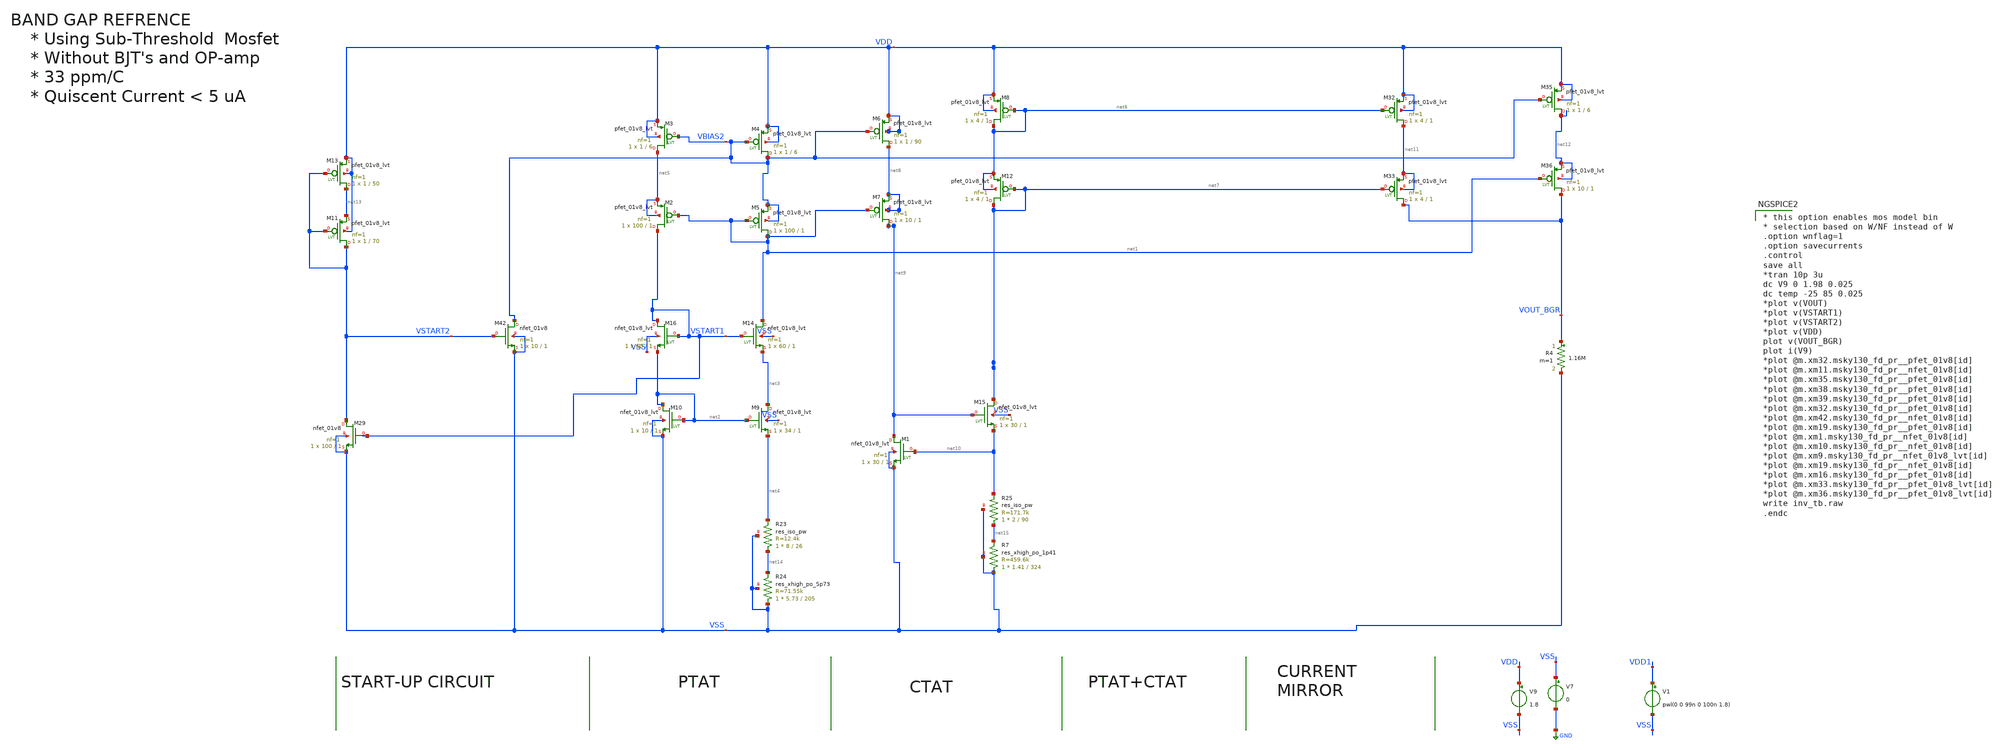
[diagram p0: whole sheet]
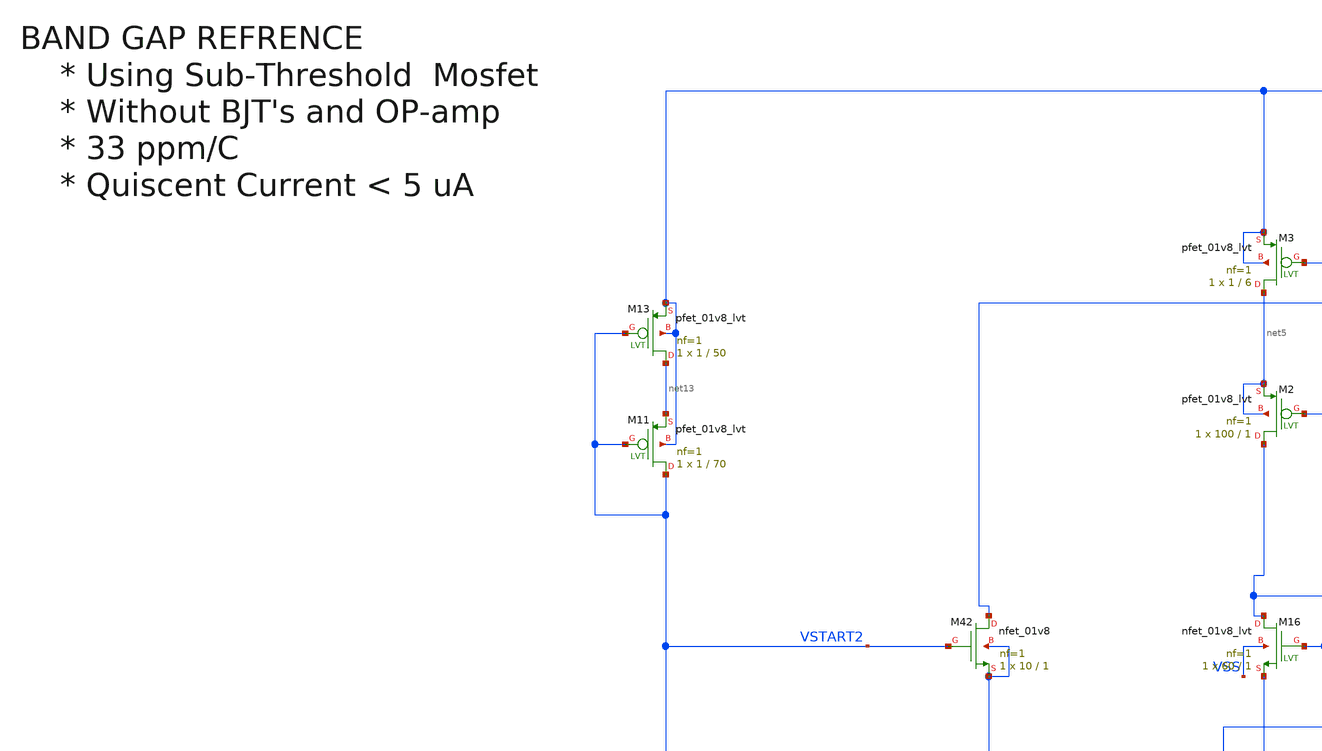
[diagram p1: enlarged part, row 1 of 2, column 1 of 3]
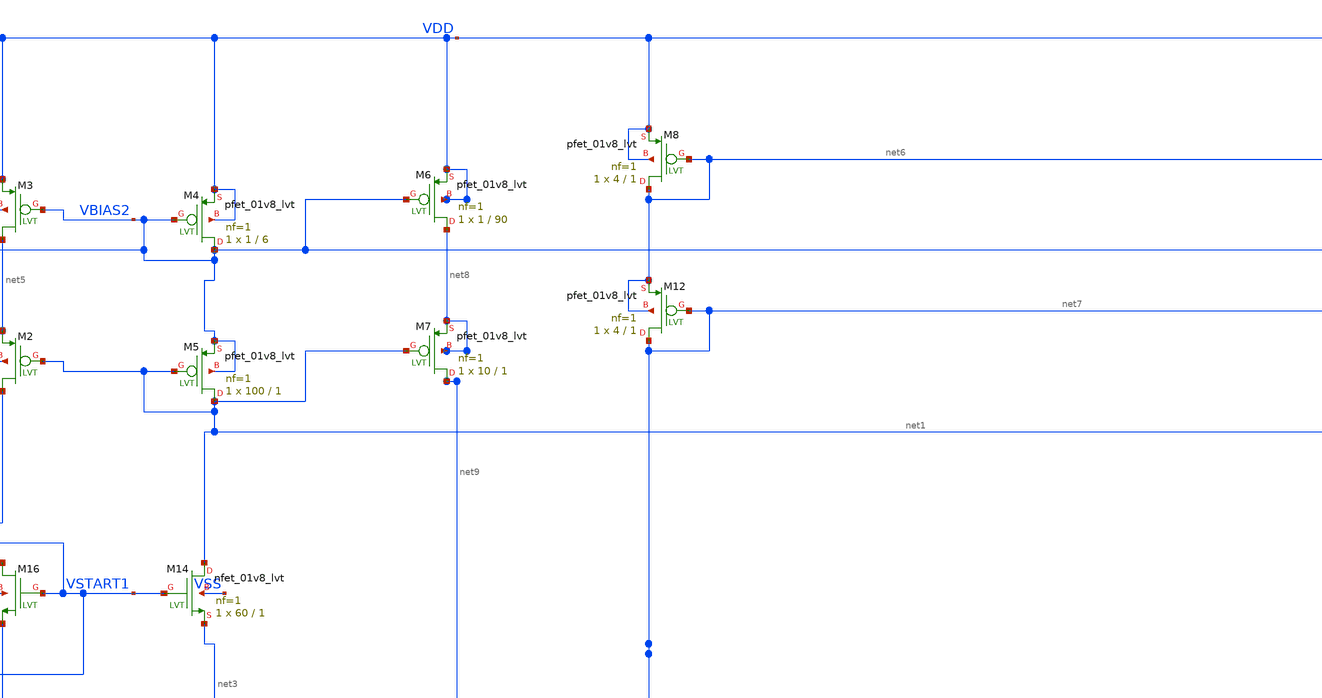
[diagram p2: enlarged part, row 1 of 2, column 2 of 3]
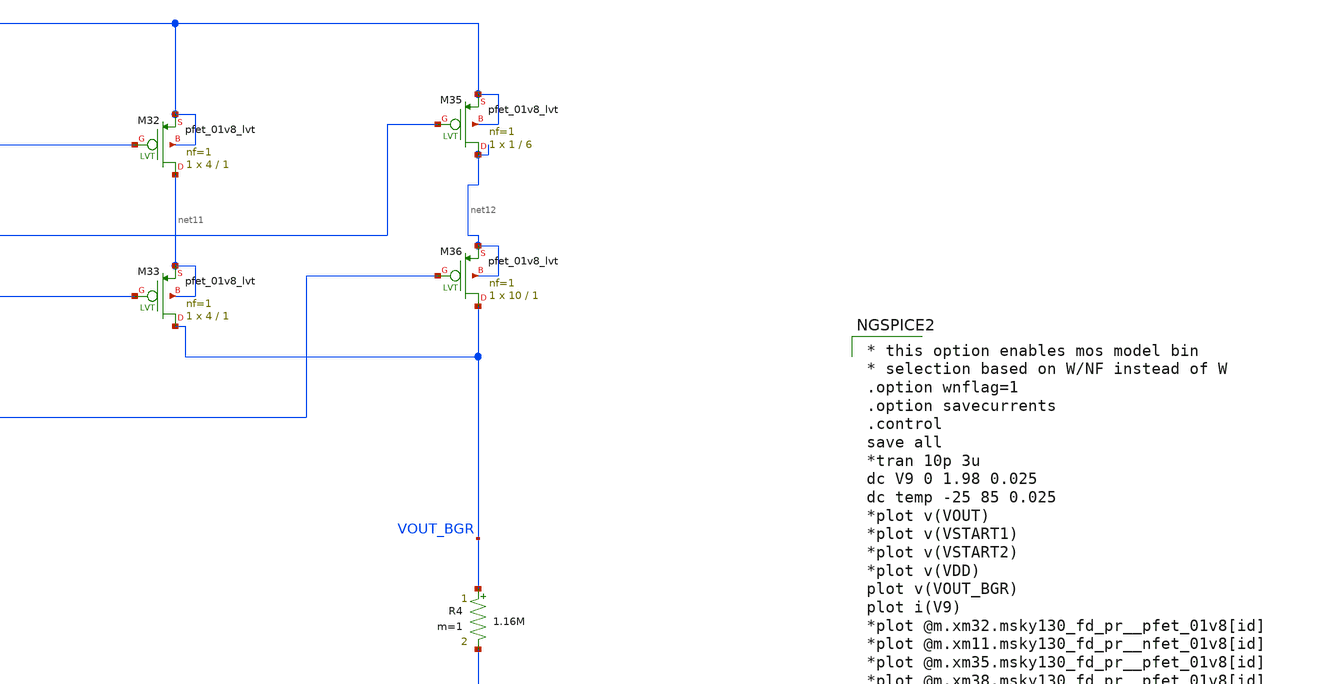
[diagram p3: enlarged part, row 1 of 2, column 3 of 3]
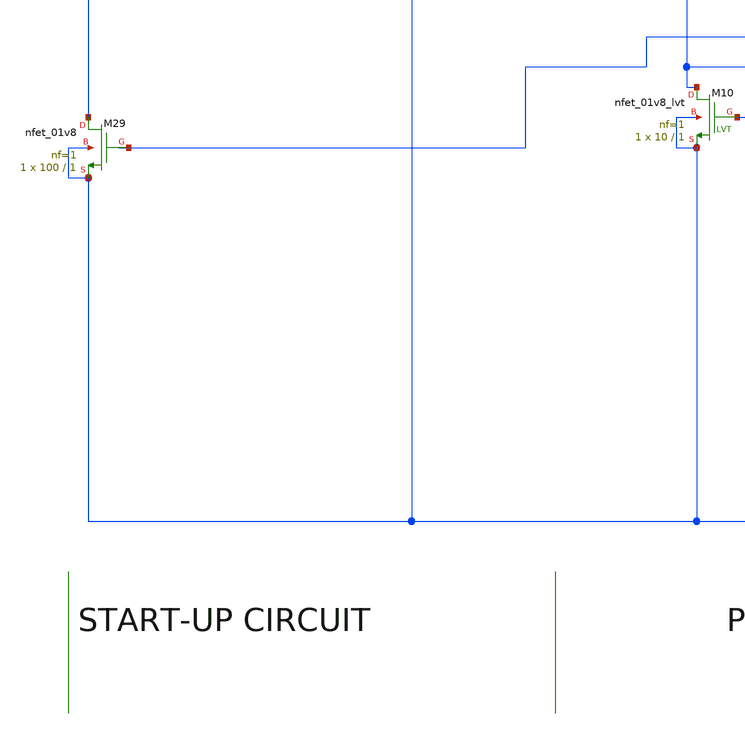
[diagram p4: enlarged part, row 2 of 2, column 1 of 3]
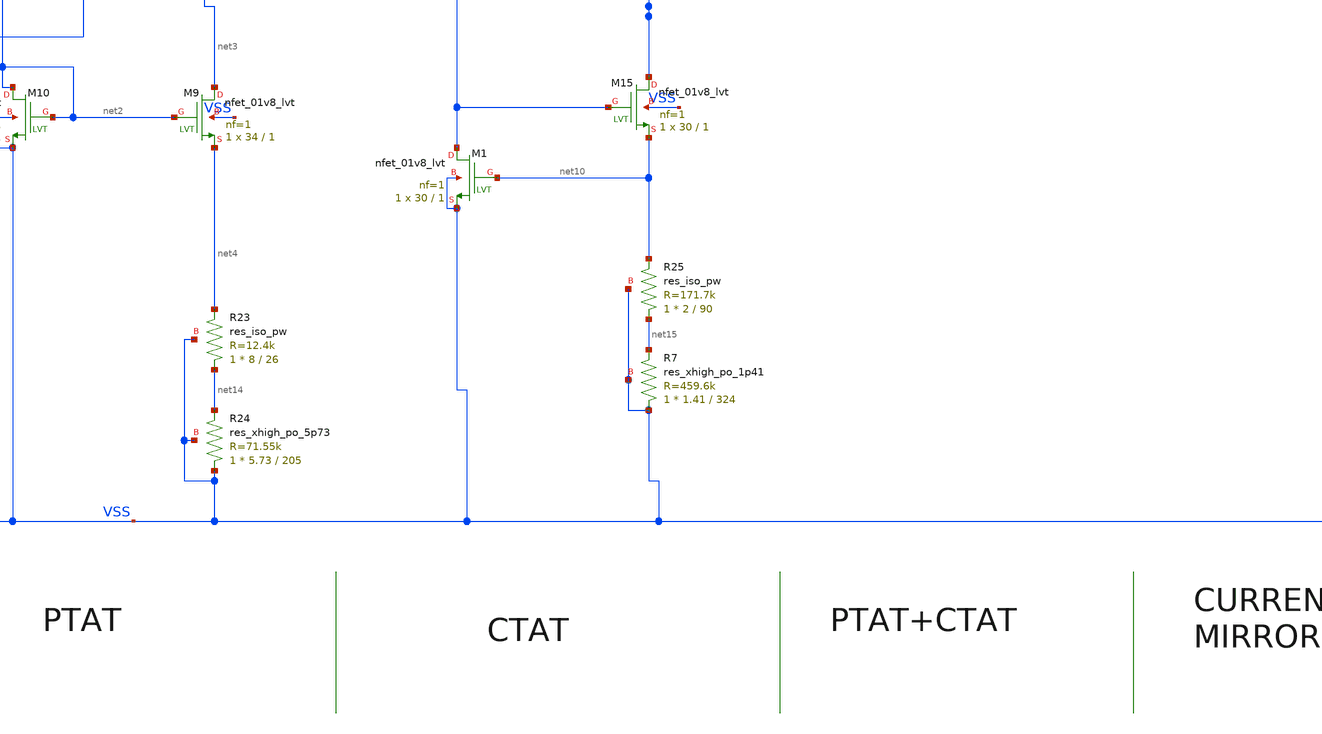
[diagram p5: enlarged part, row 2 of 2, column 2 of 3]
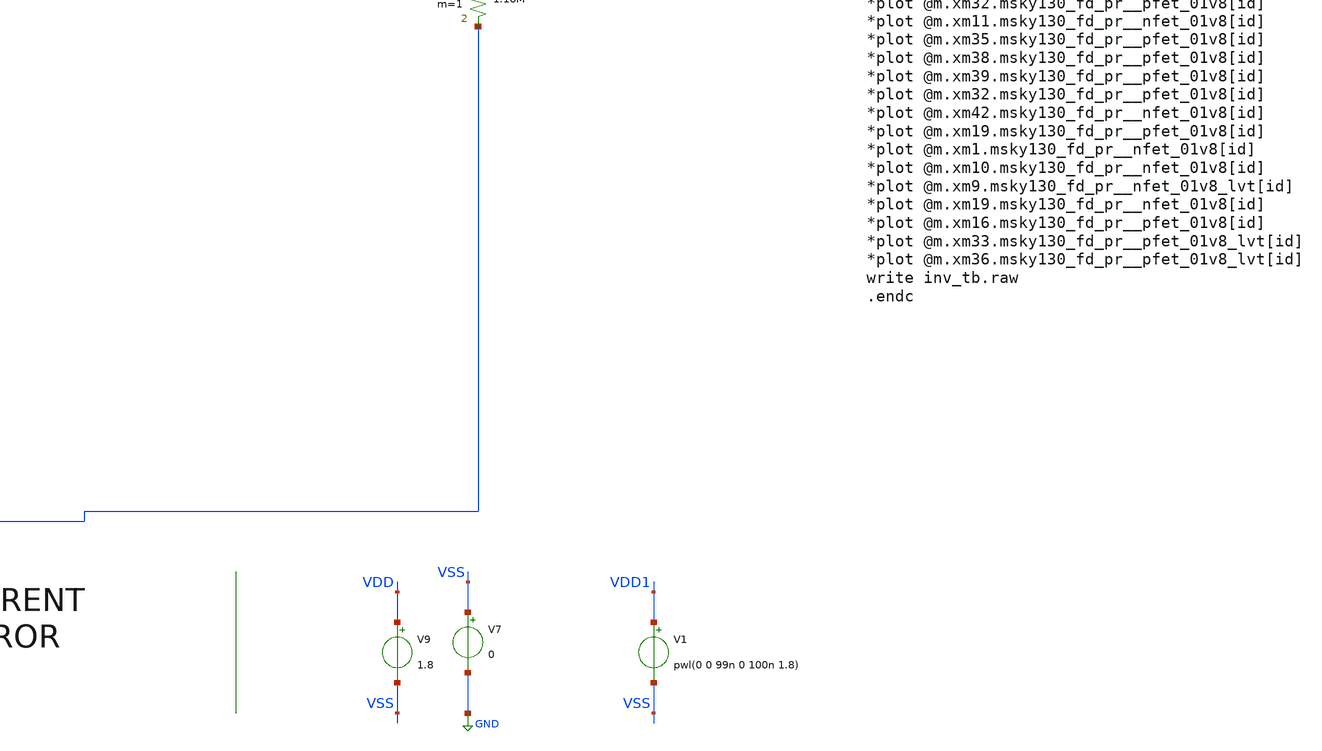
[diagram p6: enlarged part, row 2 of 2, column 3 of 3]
** sch_path: bgr_quiscent_current.sch
**.subckt bgr_quiscent_current
V7 VSS GND 0
V9 VDD VSS 1.8
XM29 VSTART2 VSTART1 VSS VSS sky130_fd_pr__nfet_01v8 L=1 W=100 nf=1 ad='int((nf+1)/2) * W/nf * 0.29'
+ as='int((nf+2)/2) * W/nf * 0.29' pd='2*int((nf+1)/2) * (W/nf + 0.29)' ps='2*int((nf+2)/2) * (W/nf + 0.29)'
+ nrd='0.29 / W' nrs='0.29 / W' sa=0 sb=0 sd=0 mult=1 m=1
XM42 VBIAS2 VSTART2 VSS VSS sky130_fd_pr__nfet_01v8 L=1 W=10 nf=1 ad='int((nf+1)/2) * W/nf * 0.29' as='int((nf+2)/2) * W/nf * 0.29'
+ pd='2*int((nf+1)/2) * (W/nf + 0.29)' ps='2*int((nf+2)/2) * (W/nf + 0.29)' nrd='0.29 / W' nrs='0.29 / W'
+ sa=0 sb=0 sd=0 mult=1 m=1
XM3 net5 VBIAS2 VDD VDD sky130_fd_pr__pfet_01v8_lvt L=6 W=1 nf=1 ad='int((nf+1)/2) * W/nf * 0.29' as='int((nf+2)/2) * W/nf * 0.29'
+ pd='2*int((nf+1)/2) * (W/nf + 0.29)' ps='2*int((nf+2)/2) * (W/nf + 0.29)' nrd='0.29 / W' nrs='0.29 / W'
+ sa=0 sb=0 sd=0 mult=1 m=1
XM2 VSTART1 net1 net5 net5 sky130_fd_pr__pfet_01v8_lvt L=1 W=100 nf=1 ad='int((nf+1)/2) * W/nf * 0.29'
+ as='int((nf+2)/2) * W/nf * 0.29' pd='2*int((nf+1)/2) * (W/nf + 0.29)' ps='2*int((nf+2)/2) * (W/nf + 0.29)'
+ nrd='0.29 / W' nrs='0.29 / W' sa=0 sb=0 sd=0 mult=1 m=1
XM4 VBIAS2 VBIAS2 VDD VDD sky130_fd_pr__pfet_01v8_lvt L=6 W=1 nf=1 ad='int((nf+1)/2) * W/nf * 0.29' as='int((nf+2)/2) * W/nf * 0.29'
+ pd='2*int((nf+1)/2) * (W/nf + 0.29)' ps='2*int((nf+2)/2) * (W/nf + 0.29)' nrd='0.29 / W' nrs='0.29 / W'
+ sa=0 sb=0 sd=0 mult=1 m=1
XM5 net1 net1 VBIAS2 VBIAS2 sky130_fd_pr__pfet_01v8_lvt L=1 W=100 nf=1 ad='int((nf+1)/2) * W/nf * 0.29'
+ as='int((nf+2)/2) * W/nf * 0.29' pd='2*int((nf+1)/2) * (W/nf + 0.29)' ps='2*int((nf+2)/2) * (W/nf + 0.29)'
+ nrd='0.29 / W' nrs='0.29 / W' sa=0 sb=0 sd=0 mult=1 m=1
XM6 net8 VBIAS2 VDD VDD sky130_fd_pr__pfet_01v8_lvt L=90 W=1 nf=1 ad='int((nf+1)/2) * W/nf * 0.29' as='int((nf+2)/2) * W/nf * 0.29'
+ pd='2*int((nf+1)/2) * (W/nf + 0.29)' ps='2*int((nf+2)/2) * (W/nf + 0.29)' nrd='0.29 / W' nrs='0.29 / W'
+ sa=0 sb=0 sd=0 mult=1 m=1
XM7 net9 net1 net8 net8 sky130_fd_pr__pfet_01v8_lvt L=1 W=10 nf=1 ad='int((nf+1)/2) * W/nf * 0.29' as='int((nf+2)/2) * W/nf * 0.29'
+ pd='2*int((nf+1)/2) * (W/nf + 0.29)' ps='2*int((nf+2)/2) * (W/nf + 0.29)' nrd='0.29 / W' nrs='0.29 / W'
+ sa=0 sb=0 sd=0 mult=1 m=1
XM8 net6 net6 VDD VDD sky130_fd_pr__pfet_01v8_lvt L=1 W=4 nf=1 ad='int((nf+1)/2) * W/nf * 0.29' as='int((nf+2)/2) * W/nf * 0.29'
+ pd='2*int((nf+1)/2) * (W/nf + 0.29)' ps='2*int((nf+2)/2) * (W/nf + 0.29)' nrd='0.29 / W' nrs='0.29 / W'
+ sa=0 sb=0 sd=0 mult=1 m=1
XM12 net7 net7 net6 net6 sky130_fd_pr__pfet_01v8_lvt L=1 W=4 nf=1 ad='int((nf+1)/2) * W/nf * 0.29' as='int((nf+2)/2) * W/nf * 0.29'
+ pd='2*int((nf+1)/2) * (W/nf + 0.29)' ps='2*int((nf+2)/2) * (W/nf + 0.29)' nrd='0.29 / W' nrs='0.29 / W'
+ sa=0 sb=0 sd=0 mult=1 m=1
XM32 net11 net6 VDD VDD sky130_fd_pr__pfet_01v8_lvt L=1 W=4 nf=1 ad='int((nf+1)/2) * W/nf * 0.29' as='int((nf+2)/2) * W/nf * 0.29'
+ pd='2*int((nf+1)/2) * (W/nf + 0.29)' ps='2*int((nf+2)/2) * (W/nf + 0.29)' nrd='0.29 / W' nrs='0.29 / W'
+ sa=0 sb=0 sd=0 mult=1 m=1
XM33 VOUT_BGR net7 net11 net11 sky130_fd_pr__pfet_01v8_lvt L=1 W=4 nf=1 ad='int((nf+1)/2) * W/nf * 0.29'
+ as='int((nf+2)/2) * W/nf * 0.29' pd='2*int((nf+1)/2) * (W/nf + 0.29)' ps='2*int((nf+2)/2) * (W/nf + 0.29)'
+ nrd='0.29 / W' nrs='0.29 / W' sa=0 sb=0 sd=0 mult=1 m=1
XM35 net12 VBIAS2 VDD VDD sky130_fd_pr__pfet_01v8_lvt L=6 W=1 nf=1 ad='int((nf+1)/2) * W/nf * 0.29' as='int((nf+2)/2) * W/nf * 0.29'
+ pd='2*int((nf+1)/2) * (W/nf + 0.29)' ps='2*int((nf+2)/2) * (W/nf + 0.29)' nrd='0.29 / W' nrs='0.29 / W'
+ sa=0 sb=0 sd=0 mult=1 m=1
XM36 VOUT_BGR net1 net12 net12 sky130_fd_pr__pfet_01v8_lvt L=1 W=10 nf=1 ad='int((nf+1)/2) * W/nf * 0.29'
+ as='int((nf+2)/2) * W/nf * 0.29' pd='2*int((nf+1)/2) * (W/nf + 0.29)' ps='2*int((nf+2)/2) * (W/nf + 0.29)'
+ nrd='0.29 / W' nrs='0.29 / W' sa=0 sb=0 sd=0 mult=1 m=1
R4 VOUT_BGR VSS 1.16M m=1
XM11 VSTART2 VSTART2 net13 VDD sky130_fd_pr__pfet_01v8_lvt L=70 W=1 nf=1 ad='int((nf+1)/2) * W/nf * 0.29'
+ as='int((nf+2)/2) * W/nf * 0.29' pd='2*int((nf+1)/2) * (W/nf + 0.29)' ps='2*int((nf+2)/2) * (W/nf + 0.29)'
+ nrd='0.29 / W' nrs='0.29 / W' sa=0 sb=0 sd=0 mult=1 m=1
XM13 net13 VSTART2 VDD VDD sky130_fd_pr__pfet_01v8_lvt L=50 W=1 nf=1 ad='int((nf+1)/2) * W/nf * 0.29'
+ as='int((nf+2)/2) * W/nf * 0.29' pd='2*int((nf+1)/2) * (W/nf + 0.29)' ps='2*int((nf+2)/2) * (W/nf + 0.29)'
+ nrd='0.29 / W' nrs='0.29 / W' sa=0 sb=0 sd=0 mult=1 m=1
V1 VDD1 VSS pwl(0 0 99n 0 100n 1.8)
XR23 net14 net4 VSS sky130_fd_pr__res_iso_pw W=8 L=26 m=1
XR24 VSS net14 VSS sky130_fd_pr__res_xhigh_po_5p73 L=205 mult=1 m=1
XR25 net15 net10 VSS sky130_fd_pr__res_iso_pw W=2 L=90 m=1
XM14 net1 VSTART1 net3 VSS sky130_fd_pr__nfet_01v8_lvt L=1 W=60 nf=1 ad='int((nf+1)/2) * W/nf * 0.29'
+ as='int((nf+2)/2) * W/nf * 0.29' pd='2*int((nf+1)/2) * (W/nf + 0.29)' ps='2*int((nf+2)/2) * (W/nf + 0.29)'
+ nrd='0.29 / W' nrs='0.29 / W' sa=0 sb=0 sd=0 mult=1 m=1
XM16 VSTART1 VSTART1 net2 VSS sky130_fd_pr__nfet_01v8_lvt L=1 W=60 nf=1 ad='int((nf+1)/2) * W/nf * 0.29'
+ as='int((nf+2)/2) * W/nf * 0.29' pd='2*int((nf+1)/2) * (W/nf + 0.29)' ps='2*int((nf+2)/2) * (W/nf + 0.29)'
+ nrd='0.29 / W' nrs='0.29 / W' sa=0 sb=0 sd=0 mult=1 m=1
XM9 net3 net2 net4 VSS sky130_fd_pr__nfet_01v8_lvt L=1 W=34 nf=1 ad='int((nf+1)/2) * W/nf * 0.29' as='int((nf+2)/2) * W/nf * 0.29'
+ pd='2*int((nf+1)/2) * (W/nf + 0.29)' ps='2*int((nf+2)/2) * (W/nf + 0.29)' nrd='0.29 / W' nrs='0.29 / W'
+ sa=0 sb=0 sd=0 mult=1 m=1
XM10 net2 net2 VSS VSS sky130_fd_pr__nfet_01v8_lvt L=1 W=10 nf=1 ad='int((nf+1)/2) * W/nf * 0.29' as='int((nf+2)/2) * W/nf * 0.29'
+ pd='2*int((nf+1)/2) * (W/nf + 0.29)' ps='2*int((nf+2)/2) * (W/nf + 0.29)' nrd='0.29 / W' nrs='0.29 / W'
+ sa=0 sb=0 sd=0 mult=1 m=1
XM1 net9 net10 VSS VSS sky130_fd_pr__nfet_01v8_lvt L=1 W=30 nf=1 ad='int((nf+1)/2) * W/nf * 0.29' as='int((nf+2)/2) * W/nf * 0.29'
+ pd='2*int((nf+1)/2) * (W/nf + 0.29)' ps='2*int((nf+2)/2) * (W/nf + 0.29)' nrd='0.29 / W' nrs='0.29 / W'
+ sa=0 sb=0 sd=0 mult=1 m=1
XM15 net7 net9 net10 VSS sky130_fd_pr__nfet_01v8_lvt L=1 W=30 nf=1 ad='int((nf+1)/2) * W/nf * 0.29' as='int((nf+2)/2) * W/nf * 0.29'
+ pd='2*int((nf+1)/2) * (W/nf + 0.29)' ps='2*int((nf+2)/2) * (W/nf + 0.29)' nrd='0.29 / W' nrs='0.29 / W'
+ sa=0 sb=0 sd=0 mult=1 m=1
XR7 VSS net15 VSS sky130_fd_pr__res_xhigh_po_1p41 L=324 mult=1 m=1
**** begin user architecture code

* this option enables mos model bin
* selection based on W/NF instead of W
.option wnflag=1
.option savecurrents
.control
save all
*tran 10p 3u
dc V9 0 1.98 0.025
dc temp -25 85 0.025
*plot v(VOUT)
*plot v(VSTART1)
*plot v(VSTART2)
*plot v(VDD)
plot v(VOUT_BGR)
plot i(V9)
*plot @m.xm32.msky130_fd_pr__pfet_01v8[id]
*plot @m.xm11.msky130_fd_pr__nfet_01v8[id]
*plot @m.xm35.msky130_fd_pr__pfet_01v8[id]
*plot @m.xm38.msky130_fd_pr__pfet_01v8[id]
*plot @m.xm39.msky130_fd_pr__pfet_01v8[id]
*plot @m.xm32.msky130_fd_pr__pfet_01v8[id]
*plot @m.xm42.msky130_fd_pr__nfet_01v8[id]
*plot @m.xm19.msky130_fd_pr__pfet_01v8[id]
*plot @m.xm1.msky130_fd_pr__nfet_01v8[id]
*plot @m.xm10.msky130_fd_pr__nfet_01v8[id]
*plot @m.xm9.msky130_fd_pr__nfet_01v8_lvt[id]
*plot @m.xm19.msky130_fd_pr__nfet_01v8[id]
*plot @m.xm16.msky130_fd_pr__pfet_01v8[id]
*plot @m.xm33.msky130_fd_pr__pfet_01v8_lvt[id]
*plot @m.xm36.msky130_fd_pr__pfet_01v8_lvt[id]
write inv_tb.raw
.endc


.lib $::SKYWATER_MODELS/sky130.lib.spice tt
**** end user architecture code
**.ends
.GLOBAL GND
.end
